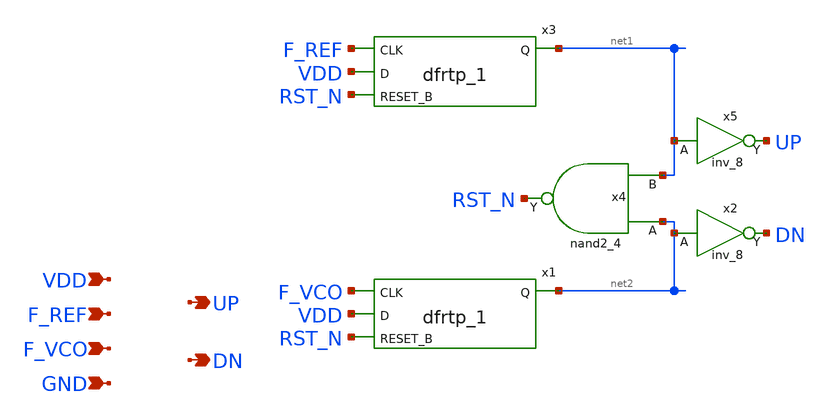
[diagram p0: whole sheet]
** sch_path: src/PFD_std.sch
**.subckt PFD_std UP F_REF VDD GND DN F_VCO
*.opin UP
*.ipin F_REF
*.ipin VDD
*.ipin GND
*.opin DN
*.ipin F_VCO
x1 F_VCO VDD RST_N GND GND VDD VDD net2 sky130_fd_sc_hd__dfrtp_1
x4 net2 net1 GND GND VDD VDD RST_N sky130_fd_sc_hd__nand2_4
x3 F_REF VDD RST_N GND GND VDD VDD net1 sky130_fd_sc_hd__dfrtp_1
x2 net2 GND GND VDD VDD DN sky130_fd_sc_hd__inv_8
x5 net1 GND GND VDD VDD UP sky130_fd_sc_hd__inv_8
**.ends
.end
